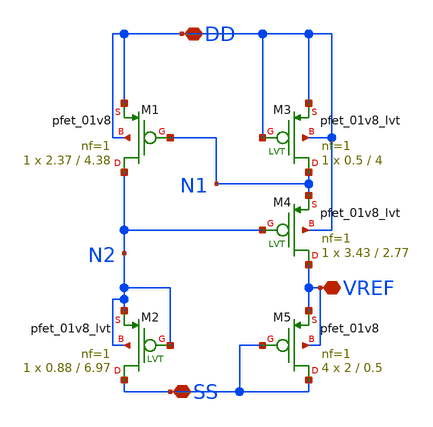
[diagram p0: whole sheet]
** sch_path: xschem/iref_2nA_vref.sch
**.subckt iref_2nA_vref DD SS VREF
*.iopin DD
*.iopin SS
*.iopin VREF
XM1 N2 N1 DD DD sky130_fd_pr__pfet_01v8 L=4.38 W=2.37 nf=1 ad='int((nf+1)/2) * W/nf * 0.29' as='int((nf+2)/2) * W/nf * 0.29'
+ pd='2*int((nf+1)/2) * (W/nf + 0.29)' ps='2*int((nf+2)/2) * (W/nf + 0.29)' nrd='0.29 / W' nrs='0.29 / W'
+ sa=0 sb=0 sd=0 mult=1 m=1
XM2 SS N2 N2 N2 sky130_fd_pr__pfet_01v8_lvt L=6.97 W=0.88 nf=1 ad='int((nf+1)/2) * W/nf * 0.29' as='int((nf+2)/2) * W/nf * 0.29'
+ pd='2*int((nf+1)/2) * (W/nf + 0.29)' ps='2*int((nf+2)/2) * (W/nf + 0.29)' nrd='0.29 / W' nrs='0.29 / W'
+ sa=0 sb=0 sd=0 mult=1 m=1
XM3 N1 DD DD DD sky130_fd_pr__pfet_01v8_lvt L=4 W=0.5 nf=1 ad='int((nf+1)/2) * W/nf * 0.29' as='int((nf+2)/2) * W/nf * 0.29'
+ pd='2*int((nf+1)/2) * (W/nf + 0.29)' ps='2*int((nf+2)/2) * (W/nf + 0.29)' nrd='0.29 / W' nrs='0.29 / W'
+ sa=0 sb=0 sd=0 mult=1 m=1
XM4 VREF N2 N1 DD sky130_fd_pr__pfet_01v8_lvt L=2.77 W=3.43 nf=1 ad='int((nf+1)/2) * W/nf * 0.29' as='int((nf+2)/2) * W/nf * 0.29'
+ pd='2*int((nf+1)/2) * (W/nf + 0.29)' ps='2*int((nf+2)/2) * (W/nf + 0.29)' nrd='0.29 / W' nrs='0.29 / W'
+ sa=0 sb=0 sd=0 mult=1 m=1
XM5 SS SS VREF VREF sky130_fd_pr__pfet_01v8 L=0.5 W=2 nf=1 ad='int((nf+1)/2) * W/nf * 0.29' as='int((nf+2)/2) * W/nf * 0.29'
+ pd='2*int((nf+1)/2) * (W/nf + 0.29)' ps='2*int((nf+2)/2) * (W/nf + 0.29)' nrd='0.29 / W' nrs='0.29 / W'
+ sa=0 sb=0 sd=0 mult=4 m=4
**.ends
.end
